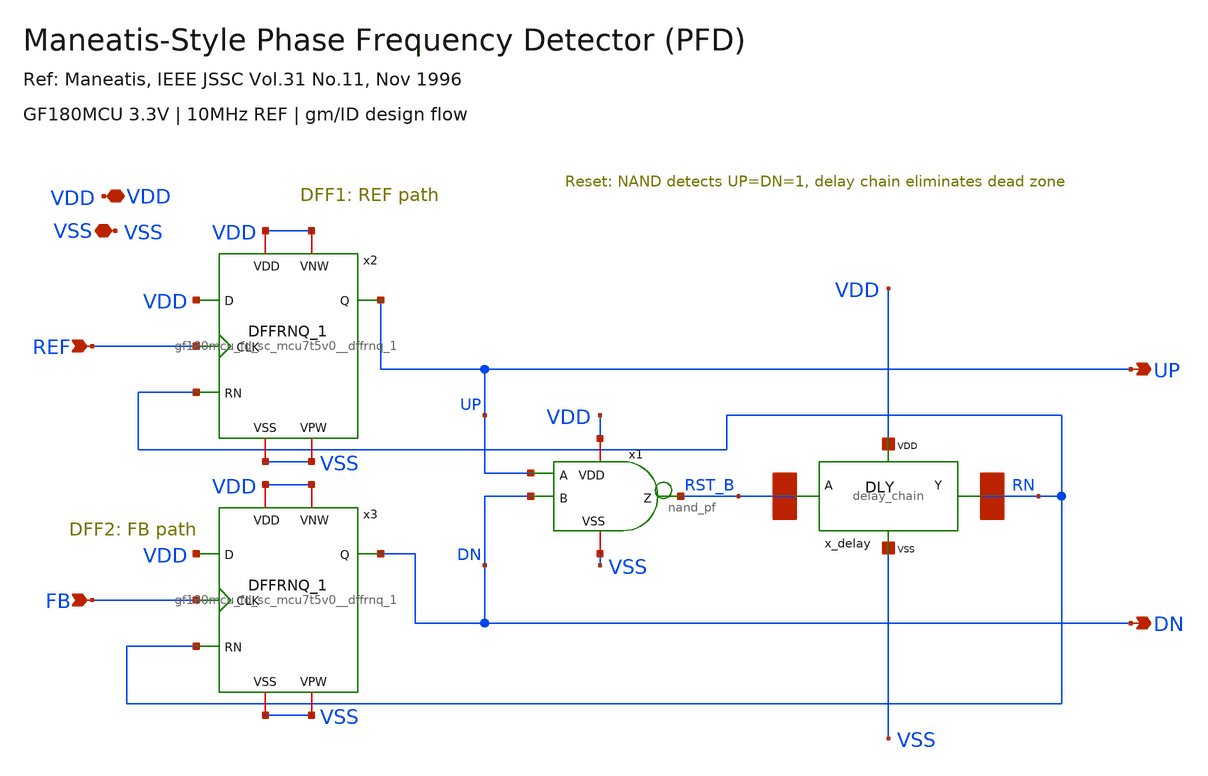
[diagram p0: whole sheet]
** sch_path: designs/libs/PDF/pfd.sch
**.subckt pfd REF FB UP DN VDD VSS
*.ipin REF
*.ipin FB
*.opin UP
*.opin DN
*.iopin VDD
*.iopin VSS
x_delay RST_B RN VDD VSS delay_chain
x1 VDD RST_B UP DN VSS nand_pf
x2 VDD RN REF UP VDD VDD VSS VSS gf180mcu_fd_sc_mcu7t5v0__dffrnq_1
x3 VDD RN FB DN VDD VDD VSS VSS gf180mcu_fd_sc_mcu7t5v0__dffrnq_1
**.ends
.end
